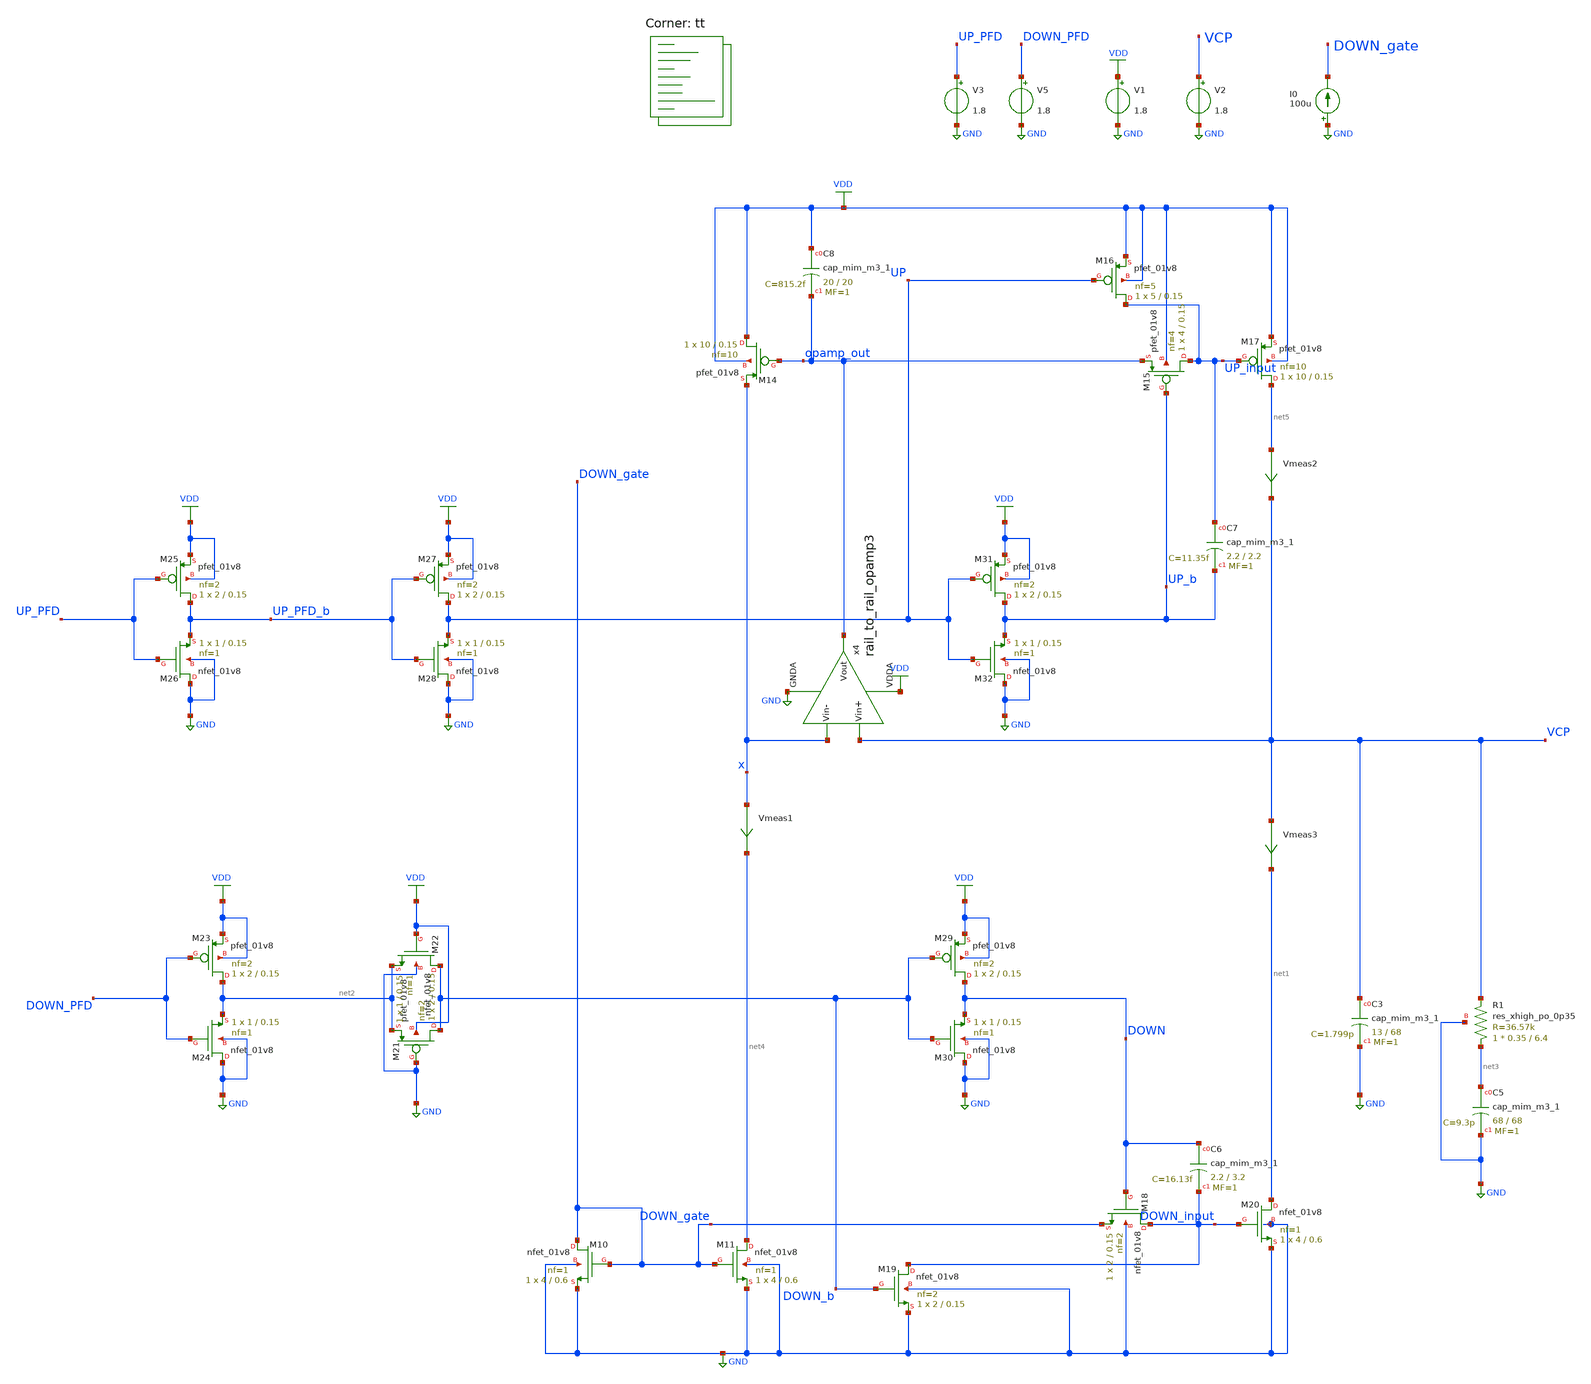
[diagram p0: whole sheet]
** sch_path: projects/pll/charge_pump/xschem_ngspice/charge_pump_DC7.sch
**.subckt charge_pump_DC7
V1 VDD GND 1.8
I0 GND DOWN_gate 100u
V3 UP_PFD GND 1.8
V5 DOWN_PFD GND 1.8
V2 VCP GND 1.8
XM10 DOWN_gate DOWN_gate GND GND sky130_fd_pr__nfet_01v8 L=0.6 W=4 nf=1 ad='int((nf+1)/2) * W/nf * 0.29'
+ as='int((nf+2)/2) * W/nf * 0.29' pd='2*int((nf+1)/2) * (W/nf + 0.29)' ps='2*int((nf+2)/2) * (W/nf + 0.29)'
+ nrd='0.29 / W' nrs='0.29 / W' sa=0 sb=0 sd=0 mult=1 m=1
XM11 net4 DOWN_gate GND GND sky130_fd_pr__nfet_01v8 L=0.6 W=4 nf=1 ad='int((nf+1)/2) * W/nf * 0.29' as='int((nf+2)/2) * W/nf * 0.29'
+ pd='2*int((nf+1)/2) * (W/nf + 0.29)' ps='2*int((nf+2)/2) * (W/nf + 0.29)' nrd='0.29 / W' nrs='0.29 / W'
+ sa=0 sb=0 sd=0 mult=1 m=1
XM14 VDD opamp_out x VDD sky130_fd_pr__pfet_01v8 L=0.15 W=10 nf=10 ad='int((nf+1)/2) * W/nf * 0.29' as='int((nf+2)/2) * W/nf * 0.29'
+ pd='2*int((nf+1)/2) * (W/nf + 0.29)' ps='2*int((nf+2)/2) * (W/nf + 0.29)' nrd='0.29 / W' nrs='0.29 / W'
+ sa=0 sb=0 sd=0 mult=1 m=1
XM15 UP_input UP_b opamp_out VDD sky130_fd_pr__pfet_01v8 L=0.15 W=4 nf=4 ad='int((nf+1)/2) * W/nf * 0.29'
+ as='int((nf+2)/2) * W/nf * 0.29' pd='2*int((nf+1)/2) * (W/nf + 0.29)' ps='2*int((nf+2)/2) * (W/nf + 0.29)'
+ nrd='0.29 / W' nrs='0.29 / W' sa=0 sb=0 sd=0 mult=1 m=1
XM16 UP_input UP VDD VDD sky130_fd_pr__pfet_01v8 L=0.15 W=5 nf=5 ad='int((nf+1)/2) * W/nf * 0.29' as='int((nf+2)/2) * W/nf * 0.29'
+ pd='2*int((nf+1)/2) * (W/nf + 0.29)' ps='2*int((nf+2)/2) * (W/nf + 0.29)' nrd='0.29 / W' nrs='0.29 / W'
+ sa=0 sb=0 sd=0 mult=1 m=1
XM17 net5 UP_input VDD VDD sky130_fd_pr__pfet_01v8 L=0.15 W=10 nf=10 ad='int((nf+1)/2) * W/nf * 0.29'
+ as='int((nf+2)/2) * W/nf * 0.29' pd='2*int((nf+1)/2) * (W/nf + 0.29)' ps='2*int((nf+2)/2) * (W/nf + 0.29)'
+ nrd='0.29 / W' nrs='0.29 / W' sa=0 sb=0 sd=0 mult=1 m=1
XM18 DOWN_input DOWN DOWN_gate GND sky130_fd_pr__nfet_01v8 L=0.15 W=2 nf=2 ad='int((nf+1)/2) * W/nf * 0.29'
+ as='int((nf+2)/2) * W/nf * 0.29' pd='2*int((nf+1)/2) * (W/nf + 0.29)' ps='2*int((nf+2)/2) * (W/nf + 0.29)'
+ nrd='0.29 / W' nrs='0.29 / W' sa=0 sb=0 sd=0 mult=1 m=1
XM19 DOWN_input DOWN_b GND GND sky130_fd_pr__nfet_01v8 L=0.15 W=2 nf=2 ad='int((nf+1)/2) * W/nf * 0.29'
+ as='int((nf+2)/2) * W/nf * 0.29' pd='2*int((nf+1)/2) * (W/nf + 0.29)' ps='2*int((nf+2)/2) * (W/nf + 0.29)'
+ nrd='0.29 / W' nrs='0.29 / W' sa=0 sb=0 sd=0 mult=1 m=1
XM20 net1 DOWN_input GND GND sky130_fd_pr__nfet_01v8 L=0.6 W=4 nf=1 ad='int((nf+1)/2) * W/nf * 0.29'
+ as='int((nf+2)/2) * W/nf * 0.29' pd='2*int((nf+1)/2) * (W/nf + 0.29)' ps='2*int((nf+2)/2) * (W/nf + 0.29)'
+ nrd='0.29 / W' nrs='0.29 / W' sa=0 sb=0 sd=0 mult=1 m=1
XC3 VCP GND sky130_fd_pr__cap_mim_m3_1 W=13 L=68 MF=1 m=1
XC5 net3 GND sky130_fd_pr__cap_mim_m3_1 W=68 L=68 MF=1 m=1
x4 VDD VCP x opamp_out GND rail_to_rail_opamp3
XR1 net3 VCP GND sky130_fd_pr__res_xhigh_po_0p35 L=6.4 mult=1 m=1
XM21 DOWN_b GND net2 VDD sky130_fd_pr__pfet_01v8 L=0.15 W=2 nf=2 ad='int((nf+1)/2) * W/nf * 0.29' as='int((nf+2)/2) * W/nf * 0.29'
+ pd='2*int((nf+1)/2) * (W/nf + 0.29)' ps='2*int((nf+2)/2) * (W/nf + 0.29)' nrd='0.29 / W' nrs='0.29 / W'
+ sa=0 sb=0 sd=0 mult=1 m=1
XM22 DOWN_b VDD net2 GND sky130_fd_pr__nfet_01v8 L=0.15 W=1 nf=1 ad='int((nf+1)/2) * W/nf * 0.29' as='int((nf+2)/2) * W/nf * 0.29'
+ pd='2*int((nf+1)/2) * (W/nf + 0.29)' ps='2*int((nf+2)/2) * (W/nf + 0.29)' nrd='0.29 / W' nrs='0.29 / W'
+ sa=0 sb=0 sd=0 mult=1 m=1
XC6 DOWN DOWN_input sky130_fd_pr__cap_mim_m3_1 W=2.2 L=3.2 MF=1 m=1
XC7 UP_input UP_b sky130_fd_pr__cap_mim_m3_1 W=2.2 L=2.2 MF=1 m=1
XC8 VDD opamp_out sky130_fd_pr__cap_mim_m3_1 W=20 L=20 MF=1 m=1
XM23 net2 DOWN_PFD VDD VDD sky130_fd_pr__pfet_01v8 L=0.15 W=2 nf=2 ad='int((nf+1)/2) * W/nf * 0.29' as='int((nf+2)/2) * W/nf * 0.29'
+ pd='2*int((nf+1)/2) * (W/nf + 0.29)' ps='2*int((nf+2)/2) * (W/nf + 0.29)' nrd='0.29 / W' nrs='0.29 / W'
+ sa=0 sb=0 sd=0 mult=1 m=1
XM24 GND DOWN_PFD net2 GND sky130_fd_pr__nfet_01v8 L=0.15 W=1 nf=1 ad='int((nf+1)/2) * W/nf * 0.29' as='int((nf+2)/2) * W/nf * 0.29'
+ pd='2*int((nf+1)/2) * (W/nf + 0.29)' ps='2*int((nf+2)/2) * (W/nf + 0.29)' nrd='0.29 / W' nrs='0.29 / W'
+ sa=0 sb=0 sd=0 mult=1 m=1
XM25 UP_PFD_b UP_PFD VDD VDD sky130_fd_pr__pfet_01v8 L=0.15 W=2 nf=2 ad='int((nf+1)/2) * W/nf * 0.29'
+ as='int((nf+2)/2) * W/nf * 0.29' pd='2*int((nf+1)/2) * (W/nf + 0.29)' ps='2*int((nf+2)/2) * (W/nf + 0.29)'
+ nrd='0.29 / W' nrs='0.29 / W' sa=0 sb=0 sd=0 mult=1 m=1
XM26 GND UP_PFD UP_PFD_b GND sky130_fd_pr__nfet_01v8 L=0.15 W=1 nf=1 ad='int((nf+1)/2) * W/nf * 0.29'
+ as='int((nf+2)/2) * W/nf * 0.29' pd='2*int((nf+1)/2) * (W/nf + 0.29)' ps='2*int((nf+2)/2) * (W/nf + 0.29)'
+ nrd='0.29 / W' nrs='0.29 / W' sa=0 sb=0 sd=0 mult=1 m=1
XM27 UP UP_PFD_b VDD VDD sky130_fd_pr__pfet_01v8 L=0.15 W=2 nf=2 ad='int((nf+1)/2) * W/nf * 0.29' as='int((nf+2)/2) * W/nf * 0.29'
+ pd='2*int((nf+1)/2) * (W/nf + 0.29)' ps='2*int((nf+2)/2) * (W/nf + 0.29)' nrd='0.29 / W' nrs='0.29 / W'
+ sa=0 sb=0 sd=0 mult=1 m=1
XM28 GND UP_PFD_b UP GND sky130_fd_pr__nfet_01v8 L=0.15 W=1 nf=1 ad='int((nf+1)/2) * W/nf * 0.29' as='int((nf+2)/2) * W/nf * 0.29'
+ pd='2*int((nf+1)/2) * (W/nf + 0.29)' ps='2*int((nf+2)/2) * (W/nf + 0.29)' nrd='0.29 / W' nrs='0.29 / W'
+ sa=0 sb=0 sd=0 mult=1 m=1
XM29 DOWN DOWN_b VDD VDD sky130_fd_pr__pfet_01v8 L=0.15 W=2 nf=2 ad='int((nf+1)/2) * W/nf * 0.29' as='int((nf+2)/2) * W/nf * 0.29'
+ pd='2*int((nf+1)/2) * (W/nf + 0.29)' ps='2*int((nf+2)/2) * (W/nf + 0.29)' nrd='0.29 / W' nrs='0.29 / W'
+ sa=0 sb=0 sd=0 mult=1 m=1
XM30 GND DOWN_b DOWN GND sky130_fd_pr__nfet_01v8 L=0.15 W=1 nf=1 ad='int((nf+1)/2) * W/nf * 0.29' as='int((nf+2)/2) * W/nf * 0.29'
+ pd='2*int((nf+1)/2) * (W/nf + 0.29)' ps='2*int((nf+2)/2) * (W/nf + 0.29)' nrd='0.29 / W' nrs='0.29 / W'
+ sa=0 sb=0 sd=0 mult=1 m=1
XM31 UP_b UP VDD VDD sky130_fd_pr__pfet_01v8 L=0.15 W=2 nf=2 ad='int((nf+1)/2) * W/nf * 0.29' as='int((nf+2)/2) * W/nf * 0.29'
+ pd='2*int((nf+1)/2) * (W/nf + 0.29)' ps='2*int((nf+2)/2) * (W/nf + 0.29)' nrd='0.29 / W' nrs='0.29 / W'
+ sa=0 sb=0 sd=0 mult=1 m=1
XM32 GND UP UP_b GND sky130_fd_pr__nfet_01v8 L=0.15 W=1 nf=1 ad='int((nf+1)/2) * W/nf * 0.29' as='int((nf+2)/2) * W/nf * 0.29'
+ pd='2*int((nf+1)/2) * (W/nf + 0.29)' ps='2*int((nf+2)/2) * (W/nf + 0.29)' nrd='0.29 / W' nrs='0.29 / W'
+ sa=0 sb=0 sd=0 mult=1 m=1
Vmeas1 x net4 0
.save i(vmeas1)
Vmeas2 net5 VCP 0
.save i(vmeas2)
Vmeas3 VCP net1 0
.save i(vmeas3)
**** begin user architecture code
.lib $::SKYWATER_MODELS/sky130.lib.spice tt



.include /foss/pdks/sky130A/libs.ref/sky130_fd_sc_hd/spice/sky130_fd_sc_hd.spice

.option method=gear trtol1
.option wnflag=1
.option savecurrents

* .temp = 75

* .ic v(vout) = 0

.save  v(up_pfd) v(down_pfd) v(up_pfd_b) v(down_pfd_b) v(up) v(up_b) v(down) v(down_b) v(v2) v(x) v(vcp) v(up_input) v(down_input) v(down_gate) v(opamp_out) v(x2.p_bias) v(x2.n_bias) v(x2.v_common_p) v(x2.v_common_n) v(x2.p_left) v(x2.p_right) v(x2.n_left) v(x2.n_right) v(f_ref) v(f_vco) v(x4.qa) v(x4.qa_b) v(x4.qb) v(x4.qb_b) v(x4.qa) v(x4.e) v(x4.e_b) v(x4.f) v(x4.f_b) v(x4.before_reset) v(x4.reset)


.control
  * save v(up_pfd) v(down_pfd) v(up_pfd_b) v(down_pfd_b) v(up) v(up_b) v(down) v(down_b) v(x)
+ v(vout) v(up_input) v(down_input)
  * save all

  * tran 1ns 10us
  dc v2 0 1.8 0.01 v3 0 1.8 1.8
  remzerovec
  write charge_pump_DC7.raw
  * wrdata /foss/designs/my_design/projects/pll/pfd/xschem_ngspice/charge_pump7_QA.txt v(osc)
  set appendwrite

.endc






**** end user architecture code
**.ends

* expanding   symbol:
*+  /foss/designs/my_design/projects/pll/charge_pump/xschem_ngspice/rail_to_rail_opamp3.sym # of pins=5
** sym_path: projects/pll/charge_pump/xschem_ngspice/rail_to_rail_opamp3.sym
** sch_path: projects/pll/charge_pump/xschem_ngspice/rail_to_rail_opamp3.sch
.subckt rail_to_rail_opamp3 VDDA Vin+ Vin- Vout GNDA
*.opin Vout
*.ipin Vin+
*.ipin Vin-
*.ipin VDDA
*.ipin GNDA
XM2 n_left Vin+ v_common_n GNDA sky130_fd_pr__nfet_01v8 L=0.15 W=1 nf=1 ad='int((nf+1)/2) * W/nf * 0.29'
+ as='int((nf+2)/2) * W/nf * 0.29' pd='2*int((nf+1)/2) * (W/nf + 0.29)' ps='2*int((nf+2)/2) * (W/nf + 0.29)'
+ nrd='0.29 / W' nrs='0.29 / W' sa=0 sb=0 sd=0 mult=1 m=1
XM3 n_right Vin- v_common_n GNDA sky130_fd_pr__nfet_01v8 L=0.15 W=1 nf=1 ad='int((nf+1)/2) * W/nf * 0.29'
+ as='int((nf+2)/2) * W/nf * 0.29' pd='2*int((nf+1)/2) * (W/nf + 0.29)' ps='2*int((nf+2)/2) * (W/nf + 0.29)'
+ nrd='0.29 / W' nrs='0.29 / W' sa=0 sb=0 sd=0 mult=1 m=1
XM5 n_left n_left VDDA VDDA sky130_fd_pr__pfet_01v8 L=0.15 W=2 nf=2 ad='int((nf+1)/2) * W/nf * 0.29'
+ as='int((nf+2)/2) * W/nf * 0.29' pd='2*int((nf+1)/2) * (W/nf + 0.29)' ps='2*int((nf+2)/2) * (W/nf + 0.29)'
+ nrd='0.29 / W' nrs='0.29 / W' sa=0 sb=0 sd=0 mult=1 m=1
XM4 n_right n_left VDDA VDDA sky130_fd_pr__pfet_01v8 L=0.15 W=2 nf=2 ad='int((nf+1)/2) * W/nf * 0.29'
+ as='int((nf+2)/2) * W/nf * 0.29' pd='2*int((nf+1)/2) * (W/nf + 0.29)' ps='2*int((nf+2)/2) * (W/nf + 0.29)'
+ nrd='0.29 / W' nrs='0.29 / W' sa=0 sb=0 sd=0 mult=1 m=1
XM6 v_common_p p_bias VDDA VDDA sky130_fd_pr__pfet_01v8 L=0.15 W=3 nf=3 ad='int((nf+1)/2) * W/nf * 0.29'
+ as='int((nf+2)/2) * W/nf * 0.29' pd='2*int((nf+1)/2) * (W/nf + 0.29)' ps='2*int((nf+2)/2) * (W/nf + 0.29)'
+ nrd='0.29 / W' nrs='0.29 / W' sa=0 sb=0 sd=0 mult=1 m=1
XM7 p_left Vin+ v_common_p VDDA sky130_fd_pr__pfet_01v8 L=0.15 W=2 nf=2 ad='int((nf+1)/2) * W/nf * 0.29'
+ as='int((nf+2)/2) * W/nf * 0.29' pd='2*int((nf+1)/2) * (W/nf + 0.29)' ps='2*int((nf+2)/2) * (W/nf + 0.29)'
+ nrd='0.29 / W' nrs='0.29 / W' sa=0 sb=0 sd=0 mult=1 m=1
XM8 p_right Vin- v_common_p VDDA sky130_fd_pr__pfet_01v8 L=0.15 W=2 nf=2 ad='int((nf+1)/2) * W/nf * 0.29'
+ as='int((nf+2)/2) * W/nf * 0.29' pd='2*int((nf+1)/2) * (W/nf + 0.29)' ps='2*int((nf+2)/2) * (W/nf + 0.29)'
+ nrd='0.29 / W' nrs='0.29 / W' sa=0 sb=0 sd=0 mult=1 m=1
XM9 p_left p_left GNDA GNDA sky130_fd_pr__nfet_01v8 L=0.15 W=1 nf=1 ad='int((nf+1)/2) * W/nf * 0.29'
+ as='int((nf+2)/2) * W/nf * 0.29' pd='2*int((nf+1)/2) * (W/nf + 0.29)' ps='2*int((nf+2)/2) * (W/nf + 0.29)'
+ nrd='0.29 / W' nrs='0.29 / W' sa=0 sb=0 sd=0 mult=1 m=1
XM10 p_right p_left GNDA GNDA sky130_fd_pr__nfet_01v8 L=0.15 W=1 nf=1 ad='int((nf+1)/2) * W/nf * 0.29'
+ as='int((nf+2)/2) * W/nf * 0.29' pd='2*int((nf+1)/2) * (W/nf + 0.29)' ps='2*int((nf+2)/2) * (W/nf + 0.29)'
+ nrd='0.29 / W' nrs='0.29 / W' sa=0 sb=0 sd=0 mult=1 m=1
XM1 v_common_n n_bias GNDA GNDA sky130_fd_pr__nfet_01v8 L=0.15 W=1 nf=1 ad='int((nf+1)/2) * W/nf * 0.29'
+ as='int((nf+2)/2) * W/nf * 0.29' pd='2*int((nf+1)/2) * (W/nf + 0.29)' ps='2*int((nf+2)/2) * (W/nf + 0.29)'
+ nrd='0.29 / W' nrs='0.29 / W' sa=0 sb=0 sd=0 mult=1 m=1
XM11 Vout n_right VDDA VDDA sky130_fd_pr__pfet_01v8 L=0.15 W=16 nf=2 ad='int((nf+1)/2) * W/nf * 0.29'
+ as='int((nf+2)/2) * W/nf * 0.29' pd='2*int((nf+1)/2) * (W/nf + 0.29)' ps='2*int((nf+2)/2) * (W/nf + 0.29)'
+ nrd='0.29 / W' nrs='0.29 / W' sa=0 sb=0 sd=0 mult=1 m=1
XM12 Vout p_right GNDA GNDA sky130_fd_pr__nfet_01v8 L=0.15 W=8 nf=1 ad='int((nf+1)/2) * W/nf * 0.29'
+ as='int((nf+2)/2) * W/nf * 0.29' pd='2*int((nf+1)/2) * (W/nf + 0.29)' ps='2*int((nf+2)/2) * (W/nf + 0.29)'
+ nrd='0.29 / W' nrs='0.29 / W' sa=0 sb=0 sd=0 mult=1 m=1
XM13 n_bias n_bias GNDA GNDA sky130_fd_pr__nfet_01v8 L=0.15 W=1 nf=1 ad='int((nf+1)/2) * W/nf * 0.29'
+ as='int((nf+2)/2) * W/nf * 0.29' pd='2*int((nf+1)/2) * (W/nf + 0.29)' ps='2*int((nf+2)/2) * (W/nf + 0.29)'
+ nrd='0.29 / W' nrs='0.29 / W' sa=0 sb=0 sd=0 mult=1 m=1
XM15 p_bias p_bias VDDA VDDA sky130_fd_pr__pfet_01v8 L=0.15 W=2 nf=2 ad='int((nf+1)/2) * W/nf * 0.29'
+ as='int((nf+2)/2) * W/nf * 0.29' pd='2*int((nf+1)/2) * (W/nf + 0.29)' ps='2*int((nf+2)/2) * (W/nf + 0.29)'
+ nrd='0.29 / W' nrs='0.29 / W' sa=0 sb=0 sd=0 mult=1 m=1
Vmeas net1 n_bias 0
.save i(vmeas)
XM14 net1 net1 p_bias p_bias sky130_fd_pr__pfet_01v8 L=0.15 W=2 nf=2 ad='int((nf+1)/2) * W/nf * 0.29'
+ as='int((nf+2)/2) * W/nf * 0.29' pd='2*int((nf+1)/2) * (W/nf + 0.29)' ps='2*int((nf+2)/2) * (W/nf + 0.29)'
+ nrd='0.29 / W' nrs='0.29 / W' sa=0 sb=0 sd=0 mult=1 m=1
.ends

.GLOBAL GND
.GLOBAL VDD
.end
